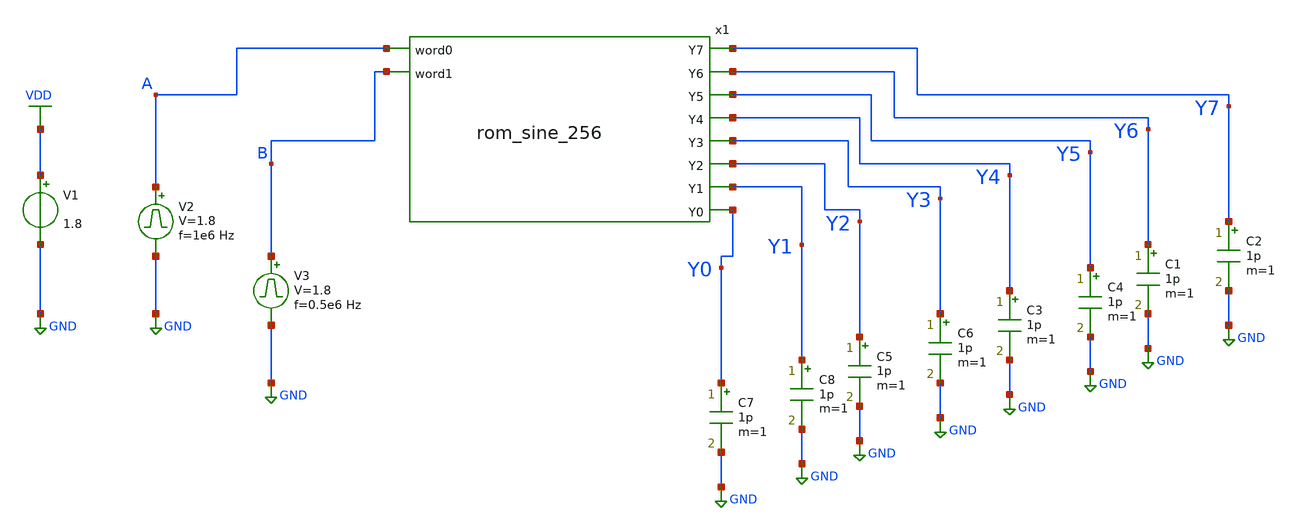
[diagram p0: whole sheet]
** sch_path: circuits/xschem/rom_sine_256_tb.sch
**.subckt rom_sine_256_tb
V1 VDD GND 1.8
V2 A GND pulse 0 1.8 '0.495/ 1e6 ' '0.01/1e6 ' '0.01/1e6 ' '0.49/1e6 ' '1/1e6 '
C1 Y6 GND 1p m=1
V3 B GND pulse 0 1.8 '0.495/ 0.5e6 ' '0.01/0.5e6 ' '0.01/0.5e6 ' '0.49/0.5e6 ' '1/0.5e6 '
C2 Y7 GND 1p m=1
C3 Y4 GND 1p m=1
C4 Y5 GND 1p m=1
C5 Y2 GND 1p m=1
C6 Y3 GND 1p m=1
C7 Y0 GND 1p m=1
C8 Y1 GND 1p m=1
x1 A B Y4 Y5 Y2 Y3 Y6 Y1 Y0 Y7 rom_sine_256
**** begin user architecture code


.control
save all
tran 1n 2u
plot V(A) V(B)+2 V(Y0)+4 V(Y1)+6 V(Y2)+8 V(Y3)+10 V(Y4)+12 V(Y5)+14 V(Y6)+16 V(Y7)+18
.endc



** opencircuitdesign pdks install
.lib $::SKYWATER_MODELS/sky130.lib.spice tt


**** end user architecture code
**.ends
.GLOBAL VDD
.GLOBAL GND
.end
